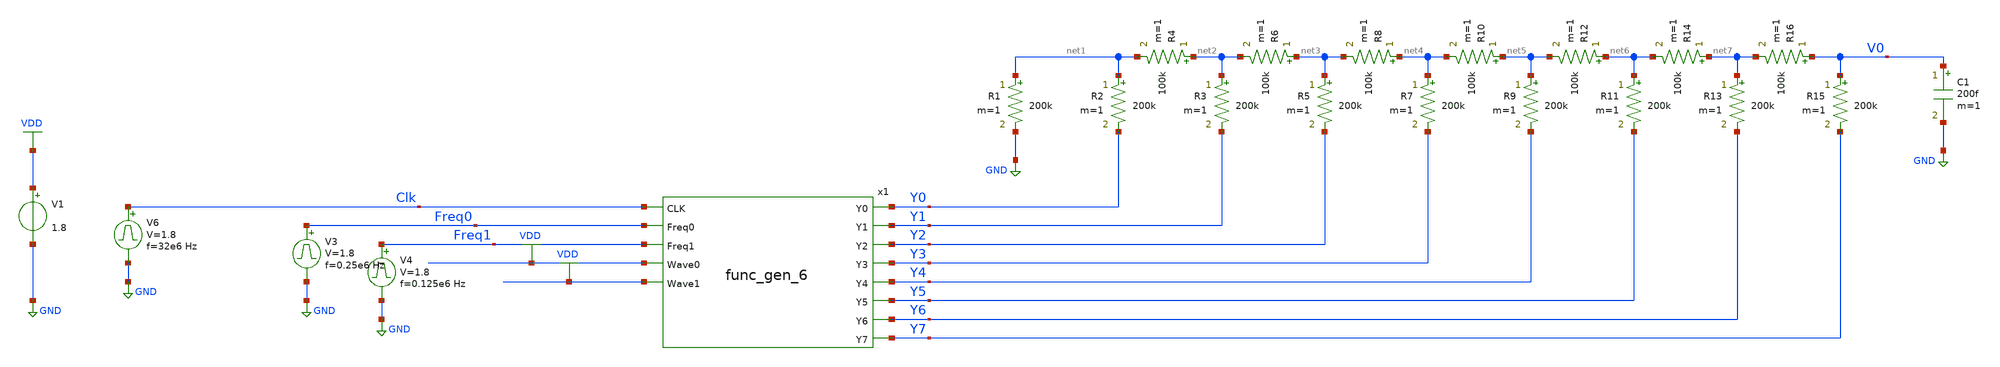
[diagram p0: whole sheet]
** sch_path: circuits/xschem/func_gen_6_freq_tb.sch
**.subckt func_gen_6_freq_tb
V1 VDD GND 1.8
V3 Freq0 GND pulse 0 1.8 '0.495/ 0.25e6 ' '0.01/0.25e6 ' '0.01/0.25e6 ' '0.49/0.25e6 ' '1/0.25e6 '
V4 Freq1 GND pulse 0 1.8 '0.495/ 0.125e6 ' '0.01/0.125e6 ' '0.01/0.125e6 ' '0.49/0.125e6 ' '1/0.125e6 '
R1 net1 GND 200k m=1
R2 net1 Y0 200k m=1
R3 net2 Y1 200k m=1
R4 net2 net1 100k m=1
R5 net3 Y2 200k m=1
R6 net3 net2 100k m=1
R7 net4 Y3 200k m=1
R8 net4 net3 100k m=1
R9 net5 Y4 200k m=1
R10 net5 net4 100k m=1
R11 net6 Y5 200k m=1
R12 net6 net5 100k m=1
R13 net7 Y6 200k m=1
R14 net7 net6 100k m=1
R15 V0 Y7 200k m=1
R16 V0 net7 100k m=1
C1 V0 GND 200f m=1
V6 Clk GND pulse 0 1.8 '0.495/ 32e6 ' '0.01/32e6 ' '0.01/32e6 ' '0.49/32e6 ' '1/32e6 '
x1 Freq1 Freq0 Y0 Clk Y1 Y2 Y3 Y4 Y5 Y6 Y7 VDD VDD func_gen_6
**** begin user architecture code


.control
save all
tran 10n 8u uic
plot V(CLK) V(Freq0)+2 V(Freq1)+4 V(V0)+6
.endc



** opencircuitdesign pdks install
.lib $::SKYWATER_MODELS/sky130.lib.spice tt


**** end user architecture code
**.ends
.GLOBAL VDD
.GLOBAL GND
.end
